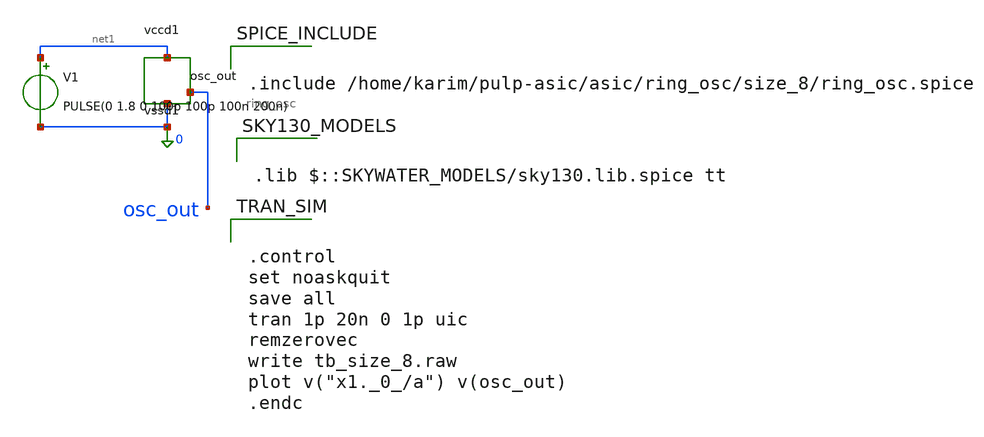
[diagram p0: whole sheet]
** sch_path: asic/ring_osc/size_8/tb_size_8.sch
**.subckt tb_size_8
X1 osc_out net1 0 ring_osc
V1 net1 0 PULSE(0 1.8 0 100p 100p 100n 200n)
**** begin user architecture code


.include /home/karim/pulp-asic/asic/ring_osc/size_8/ring_osc.spice



.lib $::SKYWATER_MODELS/sky130.lib.spice tt



.control
set noaskquit
save all
tran 1p 20n 0 1p uic
remzerovec
write tb_size_8.raw
plot v("x1._0_/a") v(osc_out)
.endc


**** end user architecture code
**.ends
.end
